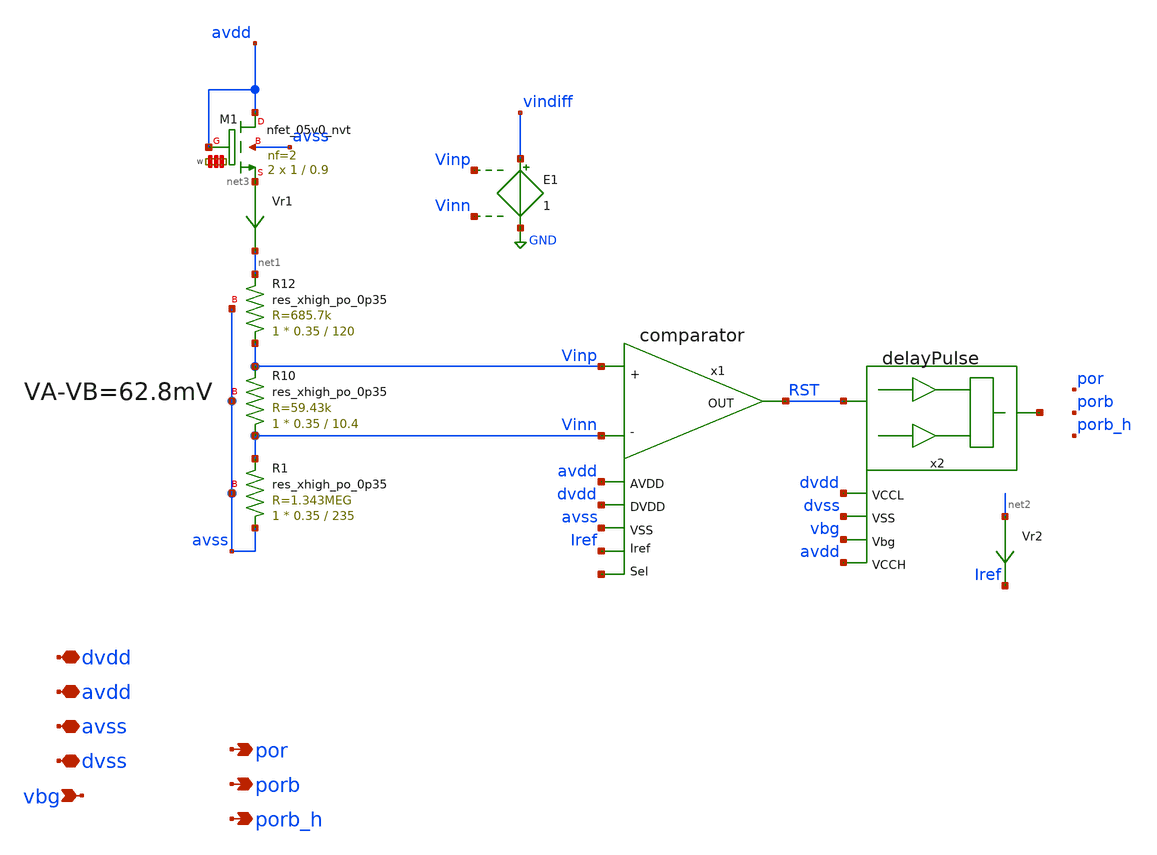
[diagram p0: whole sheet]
** sch_path: xschem/sky130_ef_ip__bgrref_por.sch
**.subckt sky130_ef_ip__bgrref_por avdd por avss dvdd porb vbg porb_h dvss
*.iopin avdd
*.opin por
*.iopin avss
*.iopin dvdd
*.opin porb
*.ipin vbg
*.opin porb_h
*.iopin dvss
XM1 avdd avdd net3 avss sky130_fd_pr__nfet_05v0_nvt L=0.9 W='1 * 2 ' nf=2 ad='int((nf+1)/2) * W / nf * 0.29'
+ as='int((nf+2)/2) * W / nf * 0.29' pd='2*int((nf+1)/2) * (W / nf + 0.29)' ps='2*int((nf+2)/2) * (W / nf + 0.29)'
+ nrd='0.29 / W ' nrs='0.29 / W ' sa=0 sb=0 sd=0 mult=2 m=2
Vr1 net3 net1 0
.save i(vr1)
E1 vindiff GND Vinp Vinn 1
x1 Iref Vinn Vinp RST avss avdd dvdd net4 comparator
XR1 avss Vinn avss sky130_fd_pr__res_xhigh_po_0p35 L=235 mult=1 m=1
XR10 Vinn Vinp avss sky130_fd_pr__res_xhigh_po_0p35 L=10.4 mult=1 m=1
XR12 Vinp net1 avss sky130_fd_pr__res_xhigh_po_0p35 L=120 mult=1 m=1
x2 RST net5 dvdd dvss vbg avdd delayPulse
Vr2 net2 Iref 0
.save i(vr2)
**.ends
.GLOBAL GND
.end
